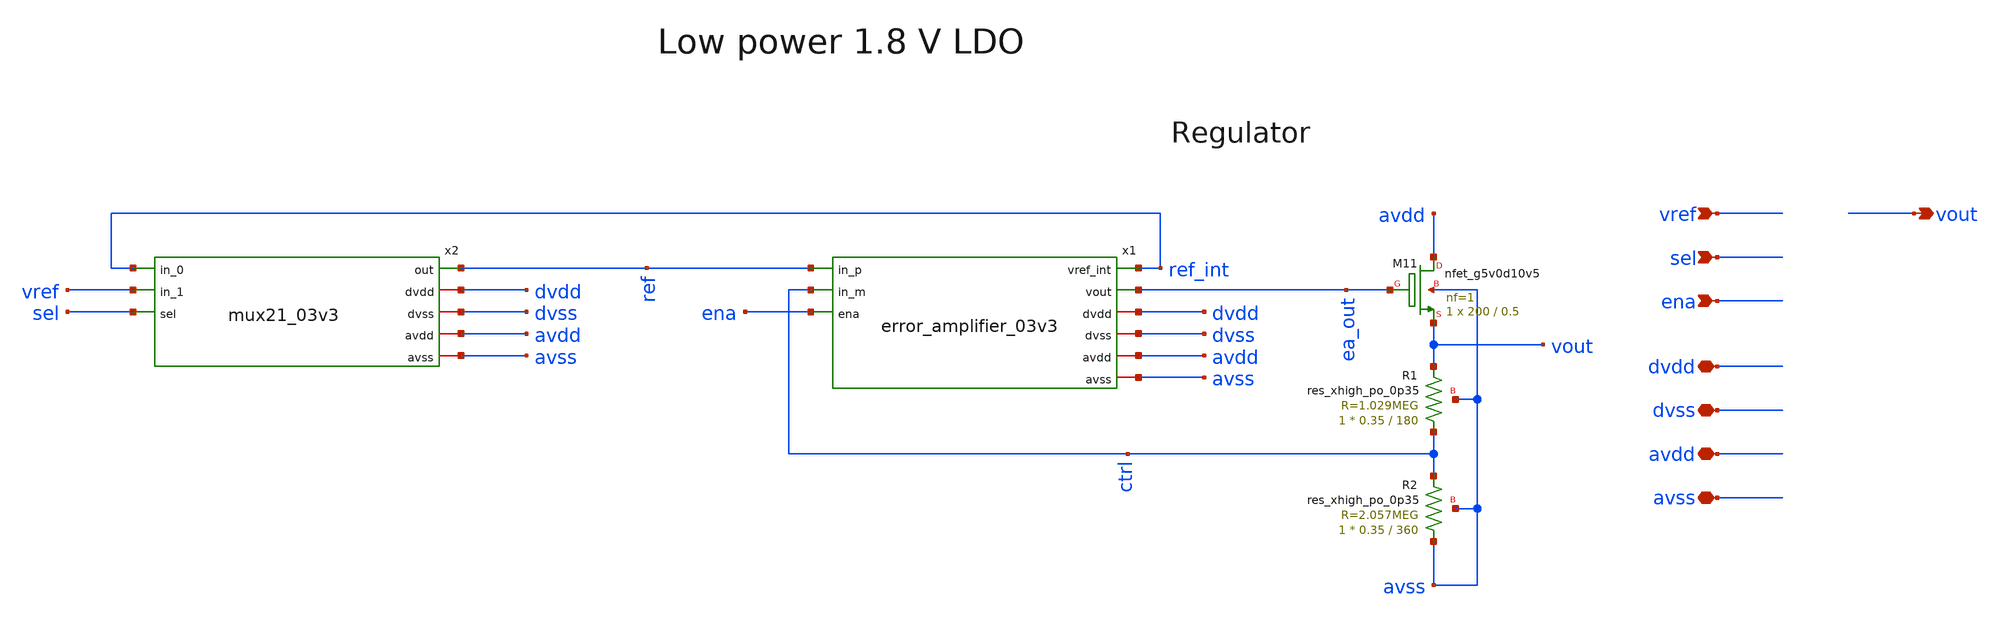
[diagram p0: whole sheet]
** sch_path: xschem/sky130_am_ip__ldo_01v8.sch
**.subckt sky130_am_ip__ldo_01v8 vout dvdd dvss ena avdd avss vref sel
*.opin vout
*.iopin dvdd
*.iopin dvss
*.ipin ena
*.iopin avdd
*.iopin avss
*.ipin vref
*.ipin sel
XM11 avdd ea_out vout avss sky130_fd_pr__nfet_g5v0d10v5 L=0.5 W=200 nf=1 ad='int((nf+1)/2) * W/nf * 0.29'
+ as='int((nf+2)/2) * W/nf * 0.29' pd='2*int((nf+1)/2) * (W/nf + 0.29)' ps='2*int((nf+2)/2) * (W/nf + 0.29)'
+ nrd='0.29 / W' nrs='0.29 / W' sa=0 sb=0 sd=0 mult=1 m=1
XR1 ctrl vout avss sky130_fd_pr__res_xhigh_po_0p35 L=180 mult=1 m=1
XR2 avss ctrl avss sky130_fd_pr__res_xhigh_po_0p35 L=360 mult=1 m=1
x1 ref_int ref ea_out ctrl ena dvdd dvss avdd avss error_amplifier_03v3
x2 ref_int ref vref sel dvdd dvss avdd avss mux21_03v3
**.ends
.end
